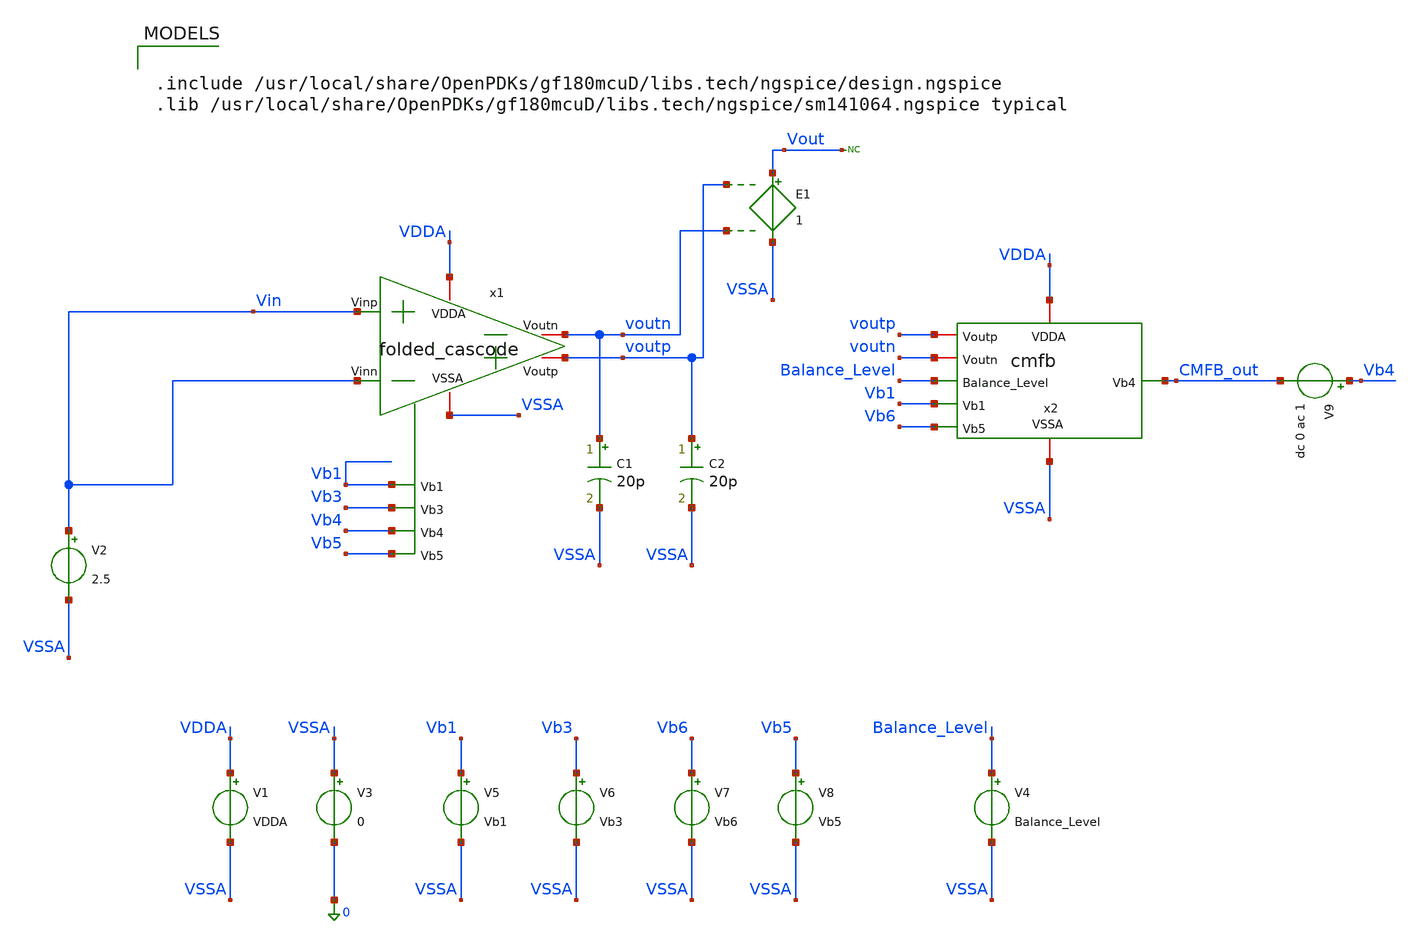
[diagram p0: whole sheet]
** sch_path: Folded_cascode/testbenches/simulation/fc_cmfb_stb_tb_batch.sch
**.subckt fc_cmfb_stb_tb_batch
x1 VDDA VSSA Vin Vin voutp voutn Vb1 Vb3 Vb4 Vb5 folded_cascode
x2 VDDA VSSA voutp voutn Balance_Level Vb1 CMFB_out Vb6 cmfb
V2 Vin VSSA 2.5
C1 voutn VSSA 20p m=1
C2 voutp VSSA 20p m=1
V1 VDDA VSSA VDDA
V3 VSSA 0 0
V5 Vb1 VSSA Vb1
V6 Vb3 VSSA Vb3
V4 Balance_Level VSSA Balance_Level
E1 Vout VSSA voutp voutn 1
* noconn Vout
V9 Vb4 CMFB_out dc 0 ac 1
V8 Vb5 VSSA Vb5
V7 Vb6 VSSA Vb6
**** begin user architecture code

.include /usr/local/share/OpenPDKs/gf180mcuD/libs.tech/ngspice/design.ngspice
.lib /usr/local/share/OpenPDKs/gf180mcuD/libs.tech/ngspice/sm141064.ngspice typical



.temp 27
.param VDDA = 5
.param Balance_Level = 1.3
.param Vb1 = 3.96
.param Vb3 = 3.6
.param Vb5 = 0.72
.param Vb6 = 0.83
.param VD = 0

.control
option sparse
set filetype=ascii
set wr_singlescale
set wr_vecnames
save all
save @m.x1.xm1.m0[id]
save @m.x1.xm1.m0[gm]
save @m.x1.xm1.m0[vgs]
save @m.x1.xm1.m0[vds]
save @m.x1.xm1.m0[vth]
save @m.x1.xm1.m0[gds]

save @m.x1.xm2.m0[id]
save @m.x1.xm2.m0[gm]
save @m.x1.xm2.m0[vgs]
save @m.x1.xm2.m0[vds]
save @m.x1.xm2.m0[vth]
save @m.x1.xm2.m0[gds]

save @m.x1.xm9.m0[id]
save @m.x1.xm9.m0[gm]
save @m.x1.xm9.m0[vgs]
save @m.x1.xm9.m0[vds]
save @m.x1.xm9.m0[vth]
save @m.x1.xm9.m0[gds]

save @m.x1.xm8.m0[id]
save @m.x1.xm8.m0[gm]
save @m.x1.xm8.m0[vgs]
save @m.x1.xm8.m0[vds]
save @m.x1.xm8.m0[vth]
save @m.x1.xm8.m0[gds]

save @m.x1.xm6.m0[id]
save @m.x1.xm6.m0[gm]
save @m.x1.xm6.m0[vgs]
save @m.x1.xm6.m0[vds]
save @m.x1.xm6.m0[vth]
save @m.x1.xm6.m0[gds]

save @m.x1.xm5.m0[id]
save @m.x1.xm5.m0[gm]
save @m.x1.xm5.m0[vgs]
save @m.x1.xm5.m0[vds]
save @m.x1.xm5.m0[vth]
save @m.x1.xm5.m0[gds]
save @m.x1.xm5.m0[vdsat]
save @m.x1.xm4.m0[vdsat]

save @m.x2.xm1.m0[id]
save @m.x2.xm1.m0[gm]
save @m.x2.xm1.m0[vgs]
save @m.x2.xm1.m0[vds]
save @m.x2.xm1.m0[vth]
save @m.x2.xm1.m0[gds]

save @m.x2.xm2.m0[id]
save @m.x2.xm2.m0[gm]
save @m.x2.xm2.m0[vgs]
save @m.x2.xm2.m0[vds]
save @m.x2.xm2.m0[vth]
save @m.x2.xm2.m0[gds]

save @m.x2.xm3.m0[id]
save @m.x2.xm3.m0[gm]
save @m.x2.xm3.m0[vgs]
save @m.x2.xm3.m0[vds]
save @m.x2.xm3.m0[vth]
save @m.x2.xm3.m0[gds]

save @m.x2.xm4.m0[id]
save @m.x2.xm4.m0[gm]
save @m.x2.xm4.m0[vgs]
save @m.x2.xm4.m0[vds]
save @m.x2.xm4.m0[vth]
save @m.x2.xm4.m0[gds]

save @m.x2.xm5.m0[id]
save @m.x2.xm5.m0[gm]
save @m.x2.xm5.m0[vgs]
save @m.x2.xm5.m0[vds]
save @m.x2.xm5.m0[vth]
save @m.x2.xm5.m0[gds]

save @m.x2.xm6.m0[id]
save @m.x2.xm6.m0[gm]
save @m.x2.xm6.m0[vgs]
save @m.x2.xm6.m0[vds]
save @m.x2.xm6.m0[vth]
save @m.x2.xm6.m0[gds]

save @m.x2.xm7.m0[id]
save @m.x2.xm7.m0[gm]
save @m.x2.xm7.m0[vgs]
save @m.x2.xm7.m0[vds]
save @m.x2.xm7.m0[vth]
save @m.x2.xm7.m0[gds]

save @m.x2.xm8.m0[id]
save @m.x2.xm8.m0[gm]
save @m.x2.xm8.m0[vgs]
save @m.x2.xm8.m0[vds]
save @m.x2.xm8.m0[vth]
save @m.x2.xm8.m0[gds]

save @m.x2.xm9.m0[id]
save @m.x2.xm9.m0[gm]
save @m.x2.xm9.m0[vgs]
save @m.x2.xm9.m0[vds]
save @m.x2.xm9.m0[vth]
save @m.x2.xm9.m0[gds]

op

write fc_cmfb_stb_op_tb.raw

set appendwrite
ac dec 100 1 1G

* Approximate CMFB loop gain
let loopgain = -v(CMFB_out)/v(Vb4)

* Magnitude and phase in degrees
let lg_db = db(loopgain)
let lg_phase_deg = phase(loopgain)*180/3.141592653589793

* -------------------------------------------------
* First 0-dB crossing
* -------------------------------------------------
meas ac f_ugf1 WHEN lg_db=0 CROSS=1
meas ac phase_ugf1 FIND lg_phase_deg AT=$&f_ugf1

let pm1 = 180 + phase_ugf1

* -------------------------------------------------
* Second 0-dB crossing
* -------------------------------------------------
meas ac f_ugf2 WHEN lg_db=0 CROSS=2
meas ac phase_ugf2 FIND lg_phase_deg AT=$&f_ugf2

* phase() wraps the phase between approximately -180 and +180 deg.
* At the second crossing, convert the positive wrapped phase
* to its continuous negative equivalent.
let phase_ugf2_unwrapped = phase_ugf2 - 360
let pm2 = 180 + phase_ugf2_unwrapped

* -------------------------------------------------
* Results
* -------------------------------------------------
print f_ugf1
print phase_ugf1
print pm1

print f_ugf2
print phase_ugf2
print phase_ugf2_unwrapped
print pm2

write fc_cmfb_stb_tb.raw

plot lg_db
plot lg_phase_deg

.endc


**** end user architecture code
**.ends
.end
